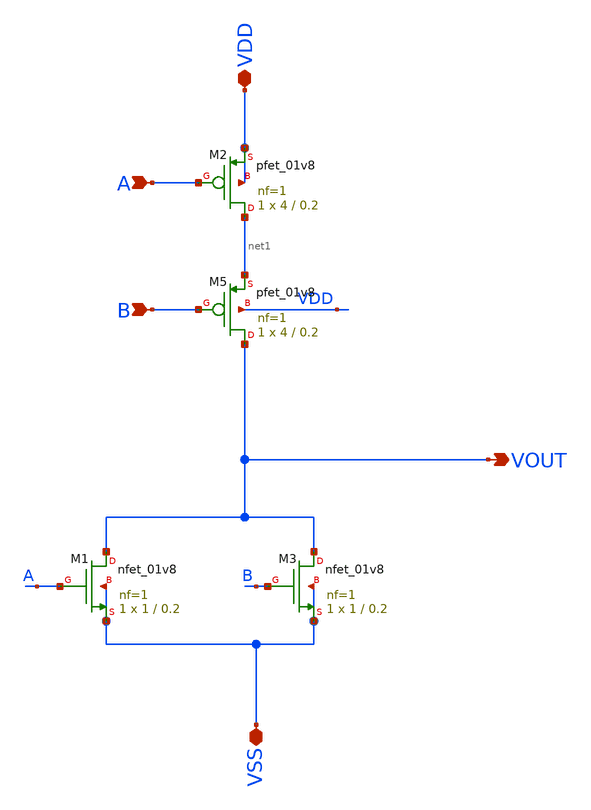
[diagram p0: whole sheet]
** sch_path: Xschem/PLL_TOP_Schematics/NOR.sch
**.subckt NOR VSS VDD A B VOUT
*.iopin VSS
*.iopin VDD
*.ipin A
*.ipin B
*.opin VOUT
XM5 VOUT B net1 VDD sky130_fd_pr__pfet_01v8 L=0.2 W=4 nf=1 ad='int((nf+1)/2) * W/nf * 0.29' as='int((nf+2)/2) * W/nf * 0.29'
+ pd='2*int((nf+1)/2) * (W/nf + 0.29)' ps='2*int((nf+2)/2) * (W/nf + 0.29)' nrd='0.29 / W' nrs='0.29 / W'
+ sa=0 sb=0 sd=0 mult=1 m=1
XM1 VOUT A VSS VSS sky130_fd_pr__nfet_01v8 L=0.2 W=1 nf=1 ad='int((nf+1)/2) * W/nf * 0.29' as='int((nf+2)/2) * W/nf * 0.29'
+ pd='2*int((nf+1)/2) * (W/nf + 0.29)' ps='2*int((nf+2)/2) * (W/nf + 0.29)' nrd='0.29 / W' nrs='0.29 / W'
+ sa=0 sb=0 sd=0 mult=1 m=1
XM2 net1 A VDD VDD sky130_fd_pr__pfet_01v8 L=0.2 W=4 nf=1 ad='int((nf+1)/2) * W/nf * 0.29' as='int((nf+2)/2) * W/nf * 0.29'
+ pd='2*int((nf+1)/2) * (W/nf + 0.29)' ps='2*int((nf+2)/2) * (W/nf + 0.29)' nrd='0.29 / W' nrs='0.29 / W'
+ sa=0 sb=0 sd=0 mult=1 m=1
XM3 VOUT B VSS VSS sky130_fd_pr__nfet_01v8 L=0.2 W=1 nf=1 ad='int((nf+1)/2) * W/nf * 0.29' as='int((nf+2)/2) * W/nf * 0.29'
+ pd='2*int((nf+1)/2) * (W/nf + 0.29)' ps='2*int((nf+2)/2) * (W/nf + 0.29)' nrd='0.29 / W' nrs='0.29 / W'
+ sa=0 sb=0 sd=0 mult=1 m=1
**.ends
.end
